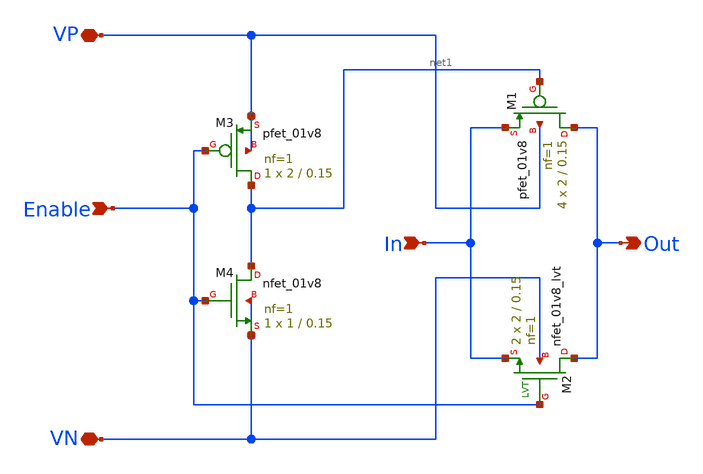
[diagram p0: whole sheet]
** sch_path: xschem/comp/switch.sch
**.subckt switch VP Enable Out VN In
*.iopin VP
*.ipin Enable
*.opin Out
*.iopin VN
*.ipin In
XM1 Out net1 In VP sky130_fd_pr__pfet_01v8 L=0.15 W=2 nf=1 ad='int((nf+1)/2) * W/nf * 0.29' as='int((nf+2)/2) * W/nf * 0.29'
+ pd='2*int((nf+1)/2) * (W/nf + 0.29)' ps='2*int((nf+2)/2) * (W/nf + 0.29)' nrd='0.29 / W' nrs='0.29 / W'
+ sa=0 sb=0 sd=0 mult=4 m=4
XM3 net1 Enable VP VP sky130_fd_pr__pfet_01v8 L=0.15 W=2 nf=1 ad='int((nf+1)/2) * W/nf * 0.29' as='int((nf+2)/2) * W/nf * 0.29'
+ pd='2*int((nf+1)/2) * (W/nf + 0.29)' ps='2*int((nf+2)/2) * (W/nf + 0.29)' nrd='0.29 / W' nrs='0.29 / W'
+ sa=0 sb=0 sd=0 mult=1 m=1
XM4 net1 Enable VN VN sky130_fd_pr__nfet_01v8 L=0.15 W=1 nf=1 ad='int((nf+1)/2) * W/nf * 0.29' as='int((nf+2)/2) * W/nf * 0.29'
+ pd='2*int((nf+1)/2) * (W/nf + 0.29)' ps='2*int((nf+2)/2) * (W/nf + 0.29)' nrd='0.29 / W' nrs='0.29 / W'
+ sa=0 sb=0 sd=0 mult=1 m=1
XM2 Out Enable In VN sky130_fd_pr__nfet_01v8_lvt L=0.15 W=2 nf=1 ad='int((nf+1)/2) * W/nf * 0.29' as='int((nf+2)/2) * W/nf * 0.29'
+ pd='2*int((nf+1)/2) * (W/nf + 0.29)' ps='2*int((nf+2)/2) * (W/nf + 0.29)' nrd='0.29 / W' nrs='0.29 / W'
+ sa=0 sb=0 sd=0 mult=2 m=2
**.ends
.end
